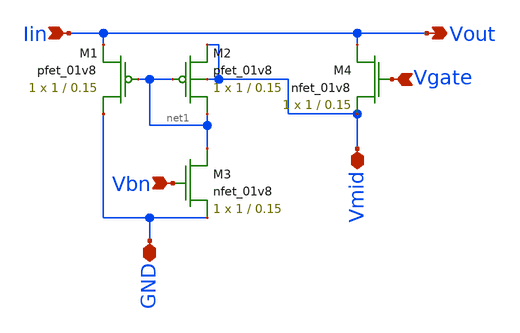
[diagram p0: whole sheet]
** sch_path: final/schematics/IV_converter.sch
**.subckt IV_converter Iin GND Vmid Vbn Vgate Vout
*.ipin Iin
*.iopin GND
*.iopin Vmid
*.ipin Vbn
*.ipin Vgate
*.opin Vout
XM1 GND net1 Iin VDD sky130_fd_pr__pfet_01v8 L=0.15 W=1 nf=1 ad='int((nf+1)/2) * W/nf * 0.29' as='int((nf+2)/2) * W/nf * 0.29'
+ pd='2*int((nf+1)/2) * (W/nf + 0.29)' ps='2*int((nf+2)/2) * (W/nf + 0.29)' nrd='0.29 / W' nrs='0.29 / W'
+ sa=0 sb=0 sd=0 mult=1 m=1
XM2 net1 net1 Vmid Vmid sky130_fd_pr__pfet_01v8 L=0.15 W=1 nf=1 ad='int((nf+1)/2) * W/nf * 0.29' as='int((nf+2)/2) * W/nf * 0.29'
+ pd='2*int((nf+1)/2) * (W/nf + 0.29)' ps='2*int((nf+2)/2) * (W/nf + 0.29)' nrd='0.29 / W' nrs='0.29 / W'
+ sa=0 sb=0 sd=0 mult=1 m=1
XM3 net1 Vbn GND GND sky130_fd_pr__nfet_01v8 L=0.15 W=1 nf=1 ad='int((nf+1)/2) * W/nf * 0.29' as='int((nf+2)/2) * W/nf * 0.29'
+ pd='2*int((nf+1)/2) * (W/nf + 0.29)' ps='2*int((nf+2)/2) * (W/nf + 0.29)' nrd='0.29 / W' nrs='0.29 / W'
+ sa=0 sb=0 sd=0 mult=1 m=1
XM4 Iin Vgate Vmid GND sky130_fd_pr__nfet_01v8 L=0.15 W=1 nf=1 ad='int((nf+1)/2) * W/nf * 0.29' as='int((nf+2)/2) * W/nf * 0.29'
+ pd='2*int((nf+1)/2) * (W/nf + 0.29)' ps='2*int((nf+2)/2) * (W/nf + 0.29)' nrd='0.29 / W' nrs='0.29 / W'
+ sa=0 sb=0 sd=0 mult=1 m=1
**.ends
.end
